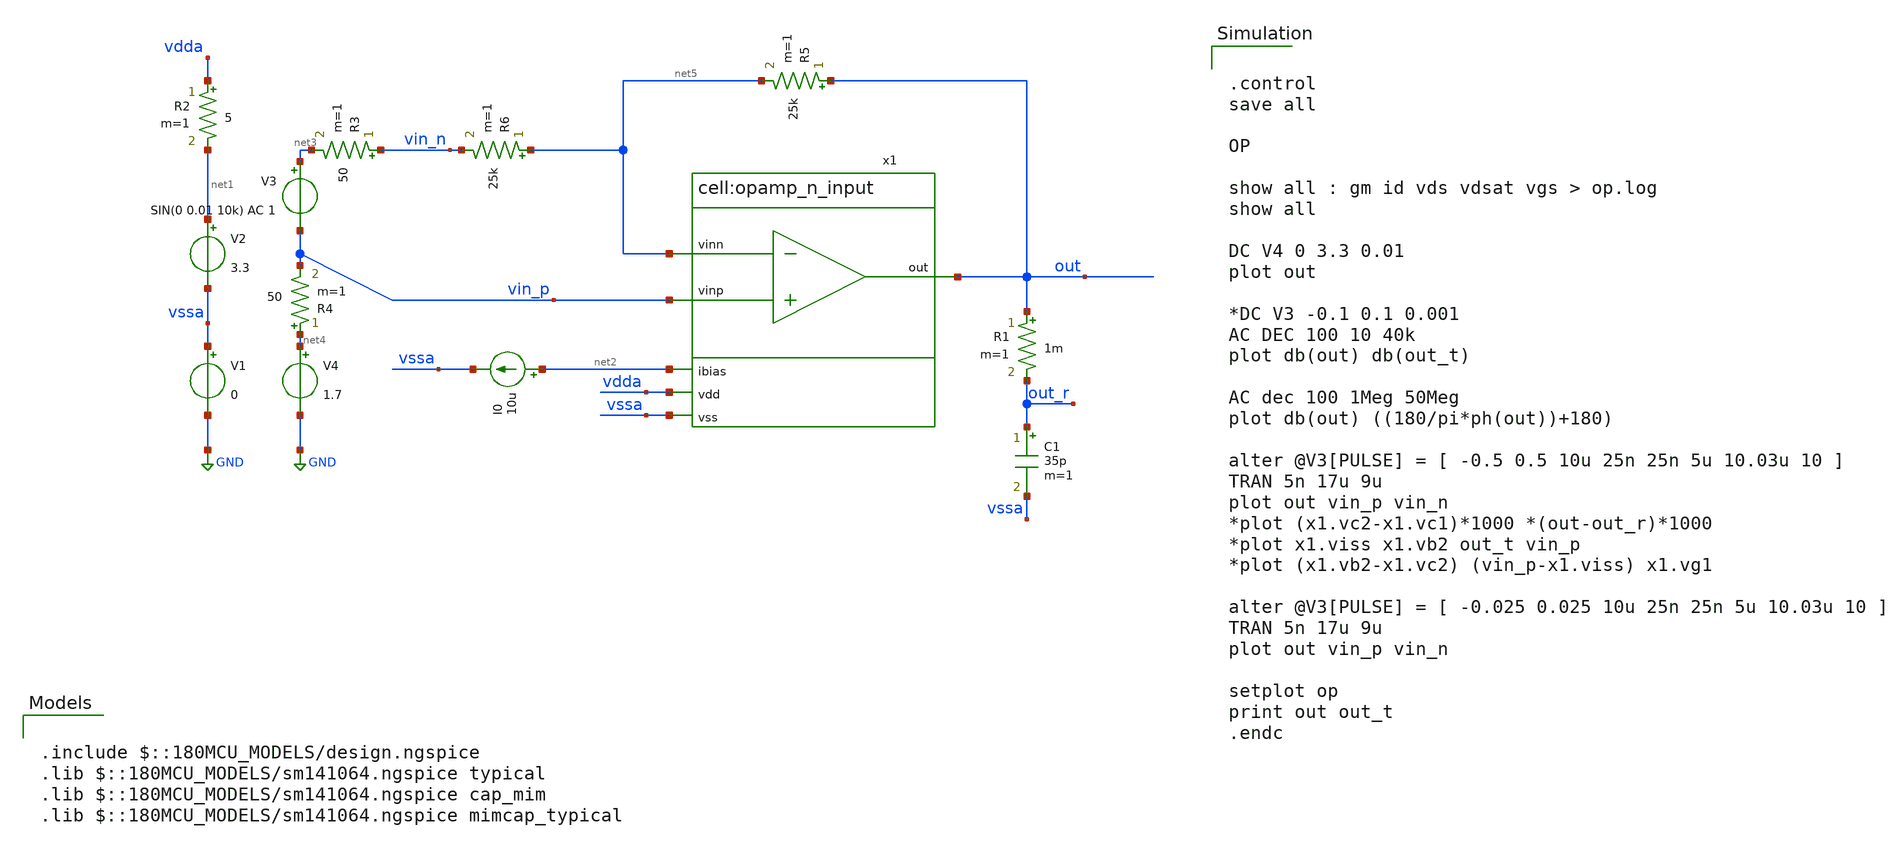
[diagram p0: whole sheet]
** sch_path: Analog/schematics/1_readout/slopedetector/2stage_OTA/opamp_n_tb.sch
**.subckt opamp_n_tb
V1 vssa GND 0
V2 net1 vssa 3.3
I0 net2 vssa 10u
V3 net3 vin_p SIN(0 0.01 10k) AC 1
V4 net4 GND 1.7
C1 out_r vssa 35p m=1
R1 out out_r 1m m=1
R2 vdda net1 5 m=1
R3 vin_n net3 50 m=1
R4 net4 vin_p 50 m=1
R5 out net5 25k m=1
R6 net5 vin_n 25k m=1
x1 vin_p net5 net2 vdda out vssa opamp_n_input
**** begin user architecture code


.control
save all

OP

show all : gm id vds vdsat vgs > op.log
show all

DC V4 0 3.3 0.01
plot out

*DC V3 -0.1 0.1 0.001
AC DEC 100 10 40k
plot db(out) db(out_t)

AC dec 100 1Meg 50Meg
plot db(out) ((180/pi*ph(out))+180)

alter @V3[PULSE] = [ -0.5 0.5 10u 25n 25n 5u 10.03u 10 ]
TRAN 5n 17u 9u
plot out vin_p vin_n
*plot (x1.vc2-x1.vc1)*1000 *(out-out_r)*1000
*plot x1.viss x1.vb2 out_t vin_p
*plot (x1.vb2-x1.vc2) (vin_p-x1.viss) x1.vg1

alter @V3[PULSE] = [ -0.025 0.025 10u 25n 25n 5u 10.03u 10 ]
TRAN 5n 17u 9u
plot out vin_p vin_n

setplot op
print out out_t
.endc



.include $::180MCU_MODELS/design.ngspice
.lib $::180MCU_MODELS/sm141064.ngspice typical
.lib $::180MCU_MODELS/sm141064.ngspice cap_mim
.lib $::180MCU_MODELS/sm141064.ngspice mimcap_typical

**** end user architecture code
**.ends
.GLOBAL GND
.end
